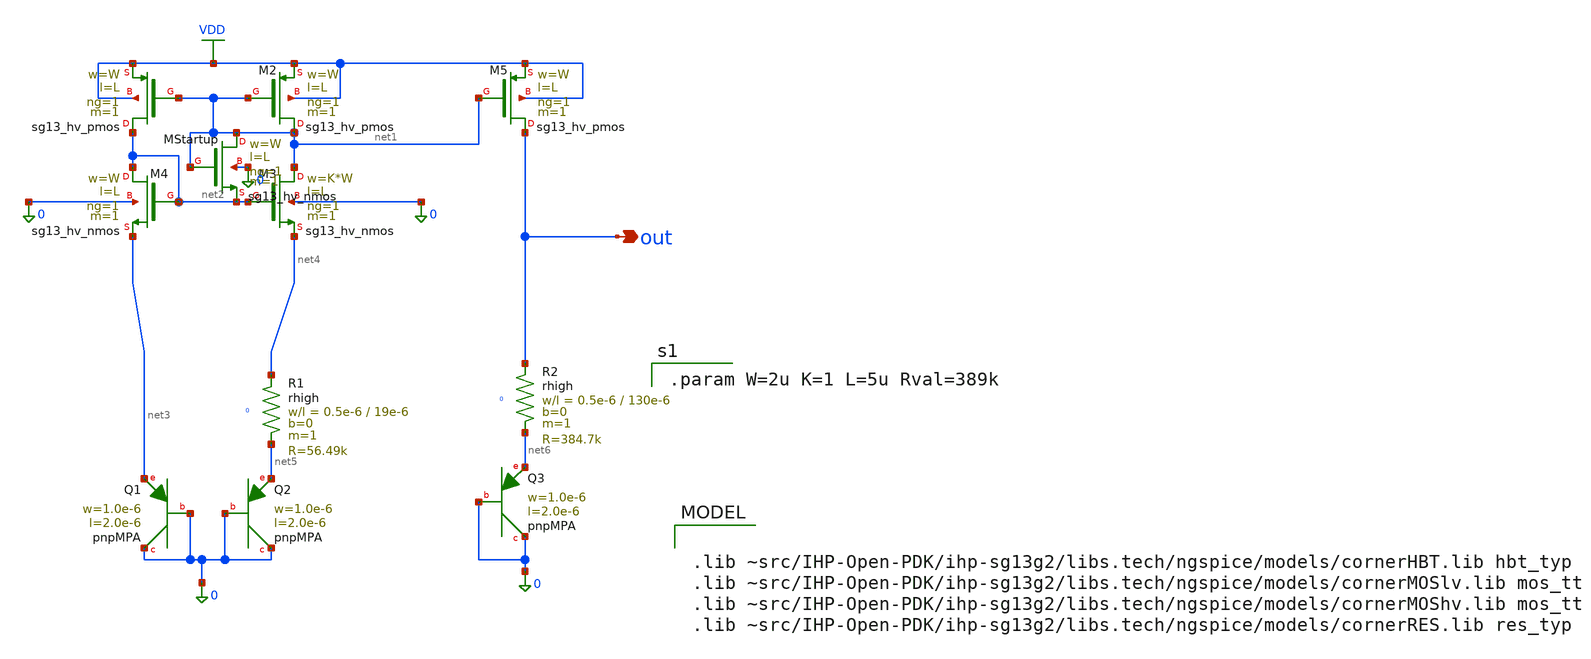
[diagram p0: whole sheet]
** sch_path: bandgap/bandgap.sch
**.subckt bandgap out
*.opin out
XM1 net2 net1 VDD VDD sg13_hv_pmos w=W l=L ng=1 m=1 mm_ok=1
XM2 net1 net1 VDD VDD sg13_hv_pmos w=W l=L ng=1 m=1 mm_ok=1
XM3 net1 net2 net4 0 sg13_hv_nmos w=K*W l=L ng=1 m=1 mm_ok=1
XM4 net2 net2 net3 0 sg13_hv_nmos w=W l=L ng=1 m=1 mm_ok=1
XQ1 0 0 net3 pnpMPA a=2p p=6u m=1
XQ2 0 0 net5 pnpMPA a=2p p=6u m=8
XM5 out net1 VDD VDD sg13_hv_pmos w=W l=L ng=1 m=1 mm_ok=1
XQ3 0 0 net6 pnpMPA a=2p p=6u m=8
XMStartup net1 net1 net2 0 sg13_hv_nmos w=W l=L ng=1 m=1 mm_ok=1
XR1 net4 net5 0 rhigh w=0.5e-6 l=19e-6 m=1 b=0 mm_ok=1
XR2 out net6 0 rhigh w=0.5e-6 l=130e-6 m=1 b=0 mm_ok=1
**** begin user architecture code

.param W=2u K=1 L=5u Rval=389k


.lib ~src/IHP-Open-PDK/ihp-sg13g2/libs.tech/ngspice/models/cornerHBT.lib hbt_typ
.lib ~src/IHP-Open-PDK/ihp-sg13g2/libs.tech/ngspice/models/cornerMOSlv.lib mos_tt
.lib ~src/IHP-Open-PDK/ihp-sg13g2/libs.tech/ngspice/models/cornerMOShv.lib mos_tt
.lib ~src/IHP-Open-PDK/ihp-sg13g2/libs.tech/ngspice/models/cornerRES.lib res_typ


**** end user architecture code
**.ends
.GLOBAL VDD
.end
